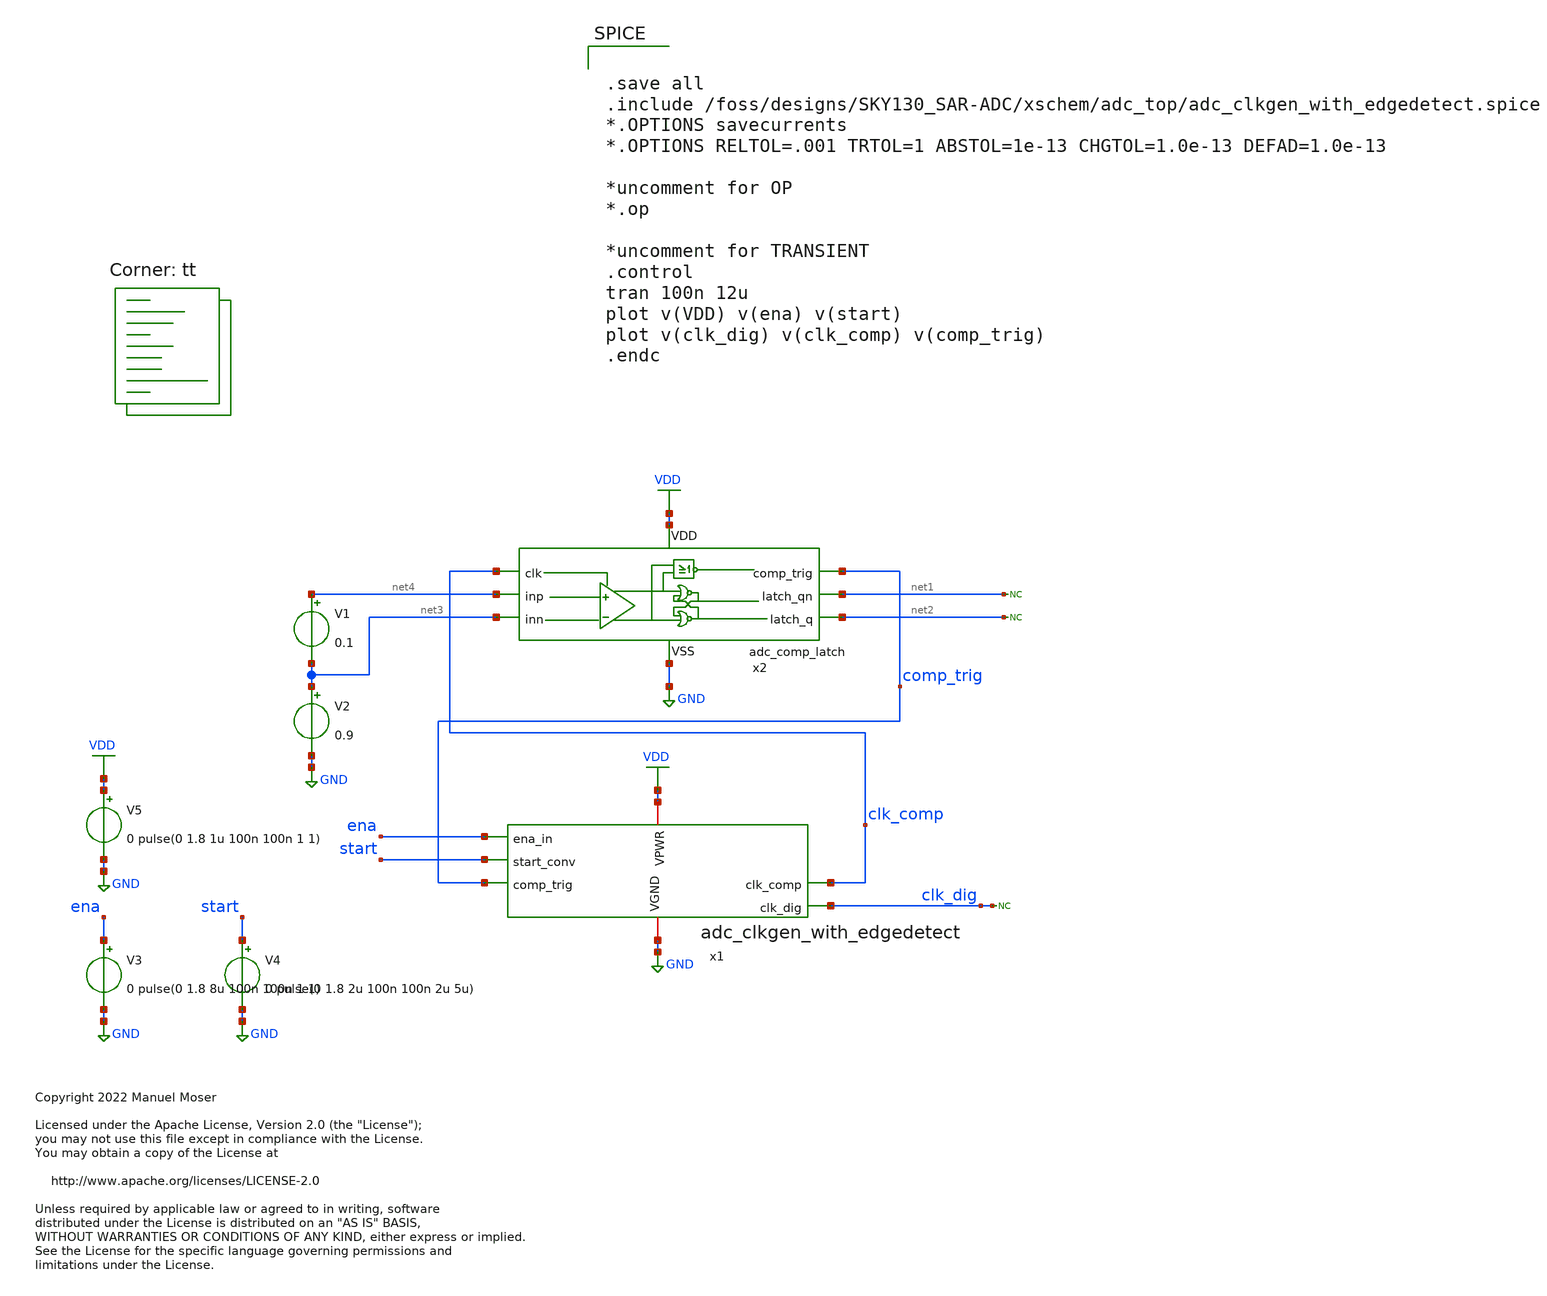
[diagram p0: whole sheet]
** sch_path: xschem/adc_top/edgedetect_with_latch_tb.sch
* Copyright 2022 Manuel Moser
* Licensed under the Apache License, Version 2.0 (the "License");
**.subckt edgedetect_with_latch_tb
x2 VDD GND comp_trig clk_comp net4 net1 net2 net3 adc_comp_latch
* noconn #net1
* noconn #net2
V1 net4 net3 0.1
V2 net3 GND 0.9
* noconn clk_dig
V3 ena GND 0 pulse(0 1.8 8u 100n 100n 1 1)
V4 start GND 0 pulse(0 1.8 2u 100n 100n 2u 5u)
V5 VDD GND 0 pulse(0 1.8 1u 100n 100n 1 1)
x1 VDD GND clk_comp clk_dig ena start comp_trig adc_clkgen_with_edgedetect
**** begin user architecture code
.lib $::SKYWATER_MODELS/sky130.lib.spice tt


.save all
.include /foss/designs/SKY130_SAR-ADC/xschem/adc_top/adc_clkgen_with_edgedetect.spice
*.OPTIONS savecurrents
*.OPTIONS RELTOL=.001 TRTOL=1 ABSTOL=1e-13 CHGTOL=1.0e-13 DEFAD=1.0e-13

*uncomment for OP
*.op

*uncomment for TRANSIENT
.control
tran 100n 12u
plot v(VDD) v(ena) v(start)
plot v(clk_dig) v(clk_comp) v(comp_trig)
.endc


**** end user architecture code
**.ends
.GLOBAL VDD
.GLOBAL GND
.end
